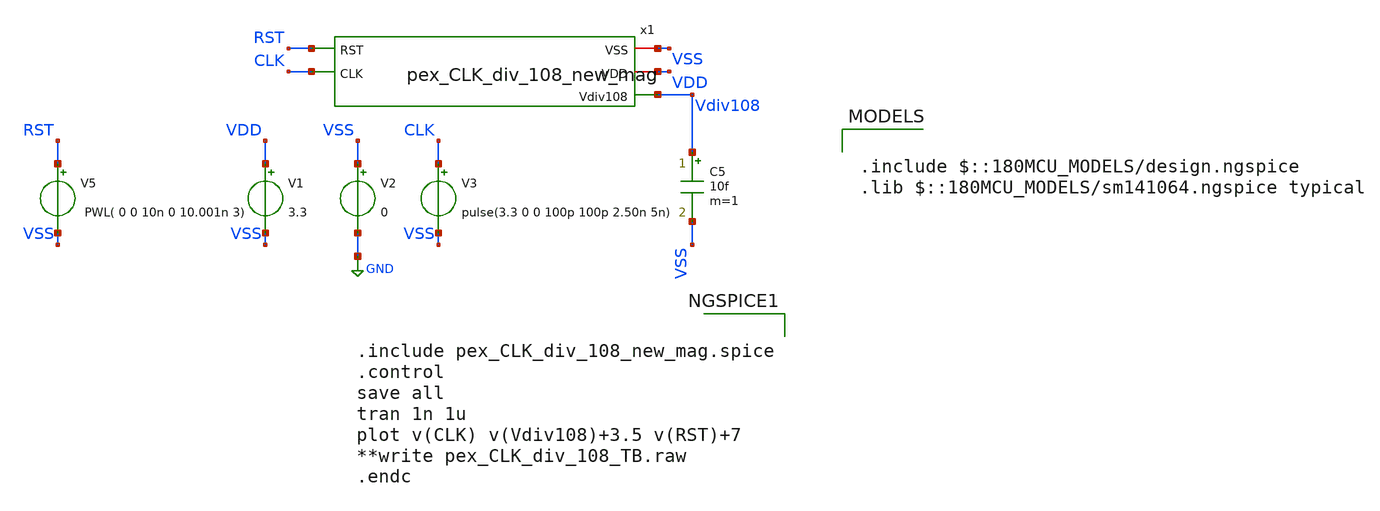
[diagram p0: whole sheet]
** sch_path: Clock_Generator_PAKISTAN_02/Schematics/pex_CLK_div_108_mag_tb.sch
**.subckt pex_CLK_div_108_mag_tb
V1 VDD VSS 3.3
V2 VSS GND 0
V3 CLK VSS pulse(3.3 0 0 100p 100p 2.50n 5n)
C5 Vdiv108 VSS 10f m=1
V5 RST VSS PWL( 0 0 10n 0 10.001n 3)
x1 VSS VDD RST Vdiv108 CLK pex_CLK_div_108_new_mag
**** begin user architecture code

.include $::180MCU_MODELS/design.ngspice
.lib $::180MCU_MODELS/sm141064.ngspice typical



.include pex_CLK_div_108_new_mag.spice
.control
save all
tran 1n 1u
plot v(CLK) v(Vdiv108)+3.5 v(RST)+7
**write pex_CLK_div_108_TB.raw
.endc


**** end user architecture code
**.ends
.GLOBAL GND
.end
